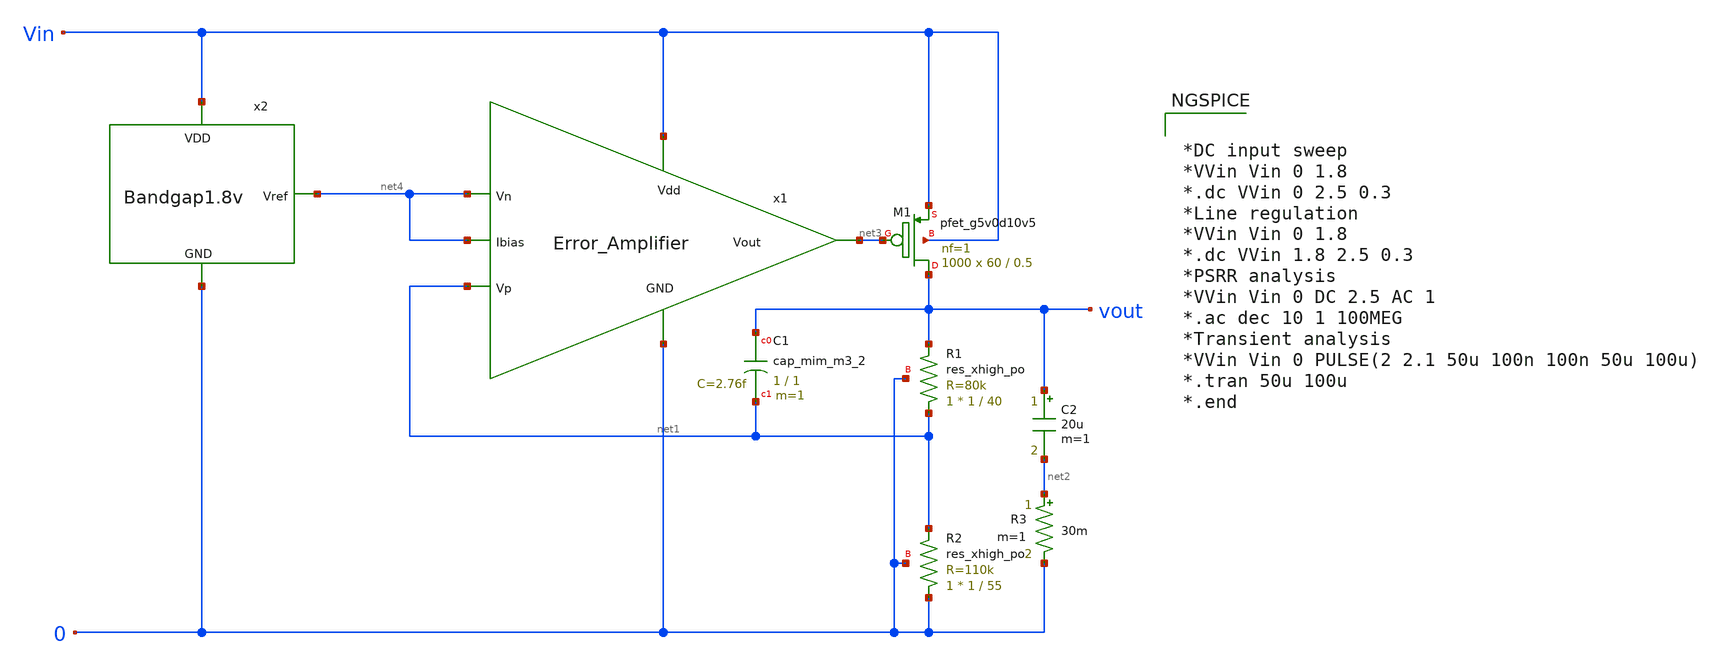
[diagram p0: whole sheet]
** sch_path: Analog_Blocks/LDO/Schematic/LDO_Miller_OTA_1.8v.sch
**.subckt LDO_Miller_OTA_1.8v
C2 vout net2 20u m=1
R3 net2 0 30m m=1
XR1 net1 vout 0 sky130_fd_pr__res_xhigh_po W=1 L=40 mult=1 m=1
XR2 0 net1 0 sky130_fd_pr__res_xhigh_po W=1 L=55 mult=1 m=1
XC1 vout net1 sky130_fd_pr__cap_mim_m3_2 W=1 L=1 MF=1 m=1
x1 Vin net4 net1 net3 net4 0 Error_Amplifier
XM1 vout net3 Vin Vin sky130_fd_pr__pfet_g5v0d10v5 L=0.5 W=60 nf=1 ad='int((nf+1)/2) * W/nf * 0.29' as='int((nf+2)/2) * W/nf * 0.29'
+ pd='2*int((nf+1)/2) * (W/nf + 0.29)' ps='2*int((nf+2)/2) * (W/nf + 0.29)' nrd='0.29 / W' nrs='0.29 / W'
+ sa=0 sb=0 sd=0 mult=1000 m=1000
x2 net4 Vin 0 Bandgap1.8v
**** begin user architecture code

.include $::SKYWATER_MODELS/cells/nfet_01v8/sky130_fd_pr__nfet_01v8__tt.corner.spice
.include $::SKYWATER_MODELS/cells/nfet_01v8_lvt/sky130_fd_pr__nfet_01v8_lvt__tt.corner.spice
.include $::SKYWATER_MODELS/cells/pfet_01v8/sky130_fd_pr__pfet_01v8__tt.corner.spice
.include $::SKYWATER_MODELS/cells/nfet_03v3_nvt/sky130_fd_pr__nfet_03v3_nvt__tt.corner.spice
.include $::SKYWATER_MODELS/cells/nfet_05v0_nvt/sky130_fd_pr__nfet_05v0_nvt__tt.corner.spice
.include $::SKYWATER_MODELS/cells/esd_nfet_01v8/sky130_fd_pr__esd_nfet_01v8__tt.corner.spice
.include $::SKYWATER_MODELS/cells/pfet_01v8_lvt/sky130_fd_pr__pfet_01v8_lvt__tt.corner.spice
.include $::SKYWATER_MODELS/cells/pfet_01v8_hvt/sky130_fd_pr__pfet_01v8_hvt__tt.corner.spice
.include $::SKYWATER_MODELS/cells/esd_pfet_g5v0d10v5/sky130_fd_pr__esd_pfet_g5v0d10v5__tt.corner.spice
.include $::SKYWATER_MODELS/cells/pfet_g5v0d10v5/sky130_fd_pr__pfet_g5v0d10v5__tt.corner.spice
.include $::SKYWATER_MODELS/cells/pfet_g5v0d16v0/sky130_fd_pr__pfet_g5v0d16v0__tt.corner.spice
.include $::SKYWATER_MODELS/cells/nfet_g5v0d10v5/sky130_fd_pr__nfet_g5v0d10v5__tt.corner.spice
.include $::SKYWATER_MODELS/cells/nfet_g5v0d16v0/sky130_fd_pr__nfet_g5v0d16v0__tt_discrete.corner.spice
.include $::SKYWATER_MODELS/cells/esd_nfet_g5v0d10v5/sky130_fd_pr__esd_nfet_g5v0d10v5__tt.corner.spice
.include $::SKYWATER_MODELS/models/corners/tt/nonfet.spice
* Mismatch parameters
.include $::SKYWATER_MODELS/cells/nfet_01v8/sky130_fd_pr__nfet_01v8__mismatch.corner.spice
.include $::SKYWATER_MODELS/cells/pfet_01v8/sky130_fd_pr__pfet_01v8__mismatch.corner.spice
.include $::SKYWATER_MODELS/cells/nfet_01v8_lvt/sky130_fd_pr__nfet_01v8_lvt__mismatch.corner.spice
.include $::SKYWATER_MODELS/cells/pfet_01v8_lvt/sky130_fd_pr__pfet_01v8_lvt__mismatch.corner.spice
.include $::SKYWATER_MODELS/cells/pfet_01v8_hvt/sky130_fd_pr__pfet_01v8_hvt__mismatch.corner.spice
.include $::SKYWATER_MODELS/cells/nfet_g5v0d10v5/sky130_fd_pr__nfet_g5v0d10v5__mismatch.corner.spice
.include $::SKYWATER_MODELS/cells/pfet_g5v0d10v5/sky130_fd_pr__pfet_g5v0d10v5__mismatch.corner.spice
.include $::SKYWATER_MODELS/cells/nfet_05v0_nvt/sky130_fd_pr__nfet_05v0_nvt__mismatch.corner.spice
.include $::SKYWATER_MODELS/cells/nfet_03v3_nvt/sky130_fd_pr__nfet_03v3_nvt__mismatch.corner.spice
* Resistor$::SKYWATER_MODELS/Capacitor
.include $::SKYWATER_MODELS/models/r+c/res_typical__cap_typical.spice
.include $::SKYWATER_MODELS/models/r+c/res_typical__cap_typical__lin.spice
* Special cells
.include $::SKYWATER_MODELS/models/corners/tt/specialized_cells.spice
* All models
.include $::SKYWATER_MODELS/models/all.spice
* Corner
.include $::SKYWATER_MODELS/models/corners/tt/rf.spice



*DC input sweep
*VVin Vin 0 1.8
*.dc VVin 0 2.5 0.3
*Line regulation
*VVin Vin 0 1.8
*.dc VVin 1.8 2.5 0.3
*PSRR analysis
*VVin Vin 0 DC 2.5 AC 1
*.ac dec 10 1 100MEG
*Transient analysis
*VVin Vin 0 PULSE(2 2.1 50u 100n 100n 50u 100u)
*.tran 50u 100u
*.end


**** end user architecture code
**.ends
.end
